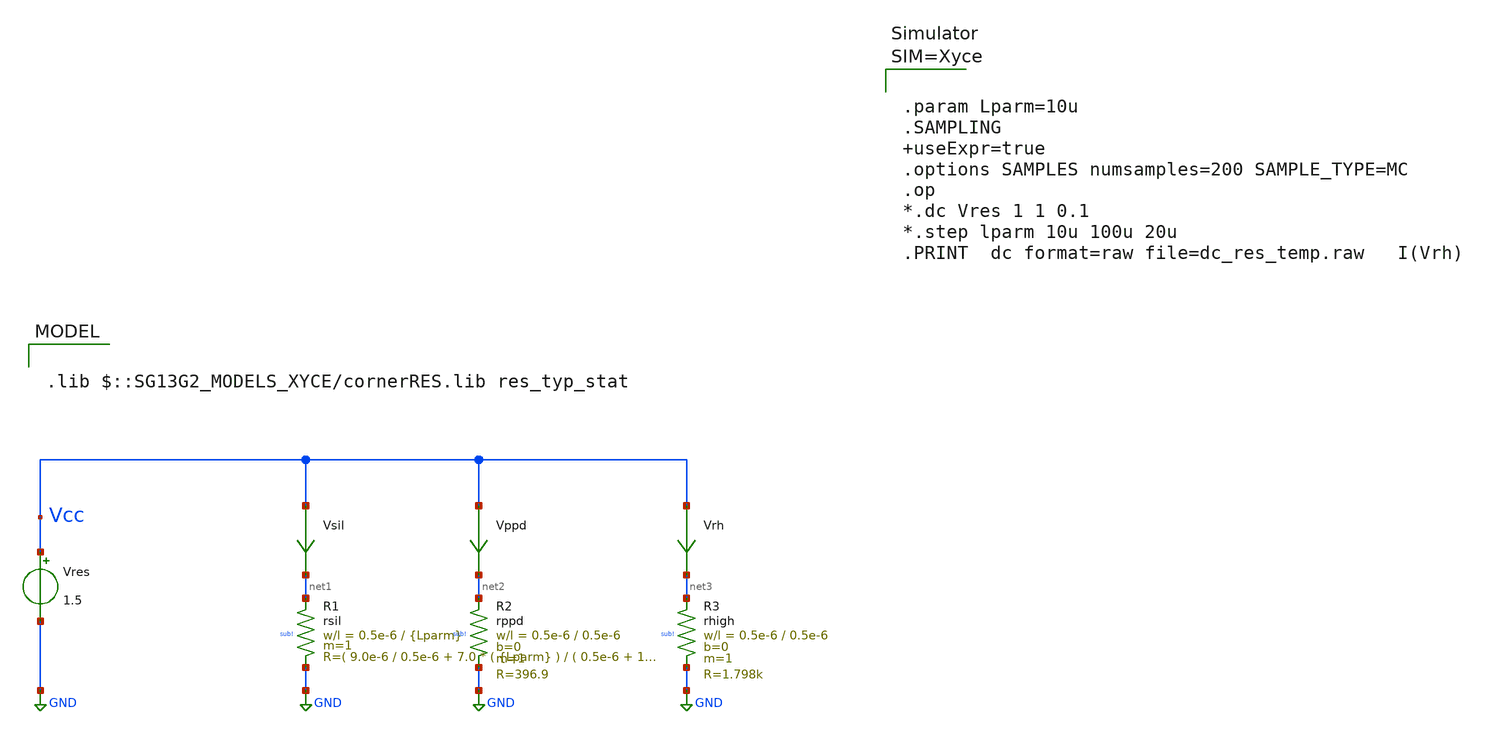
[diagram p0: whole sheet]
** sch_path: ihp-sg13g2/libs.tech/xschem/sg13g2_tests_xyce/tmp_dc_res_stats.sch
* Copyright 2023 IHP PDK Authors
**.subckt tmp_dc_res_stats
Vres Vcc GND 1.5
Vsil Vcc net1 0
.save i(vsil)
Vppd Vcc net2 0
.save i(vppd)
Vrh Vcc net3 0
.save i(vrh)
XR1 net1 GND sub! rsil w=0.5e-6 l={Lparm} m=1 mm_ok=1
XR2 net2 GND sub! rppd w=0.5e-6 l=0.5e-6 m=1 b=0 mm_ok=1
XR3 net3 GND sub! rhigh w=0.5e-6 l=0.5e-6 m=1 b=0 mm_ok=1
**** begin user architecture code

.lib $::SG13G2_MODELS_XYCE/cornerRES.lib res_typ_stat




**** end user architecture code
**.ends
.GLOBAL GND
.end
